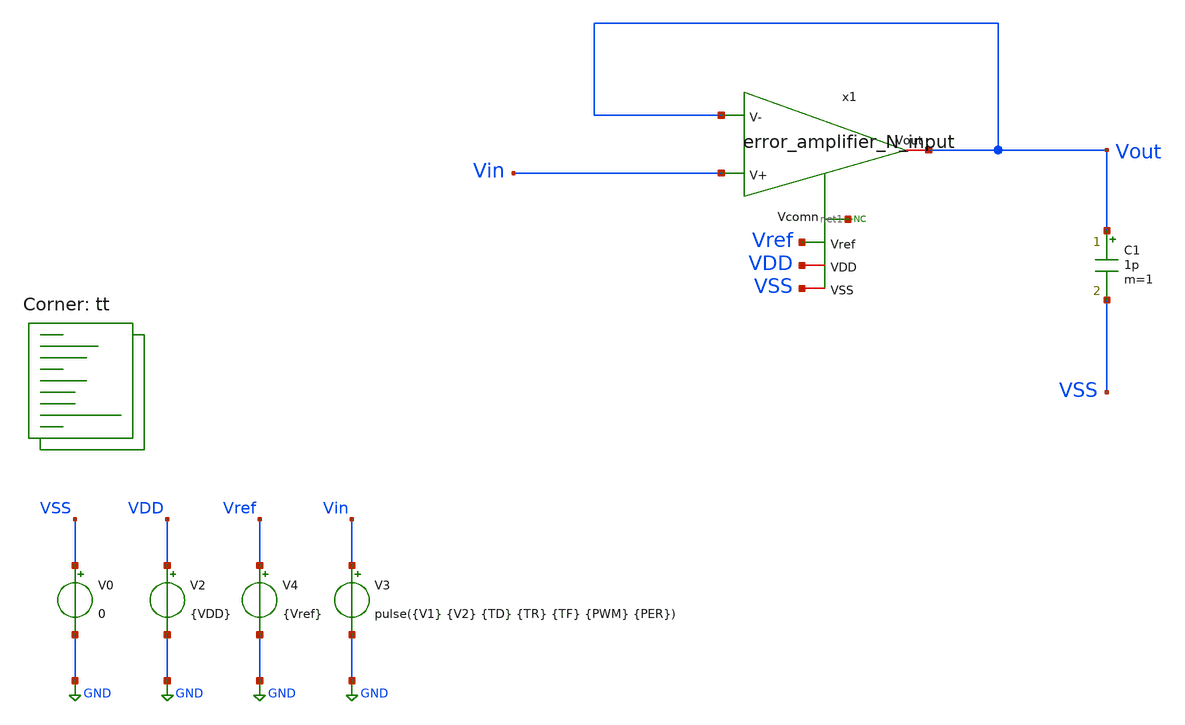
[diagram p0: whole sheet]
** sch_path: blocks/composite/folded_cascode/designs/gf180/error_amplifier_N_input/xschem/folded_cascode_sr.sch
**.subckt folded_cascode_sr
V0 VSS GND 0
V2 VDD GND {VDD}
V4 Vref GND {Vref}
C1 Vout VSS 1p m=1
* noconn #net1
V3 Vin GND pulse({V1} {V2} {TD} {TR} {TF} {PWM} {PER})
x1 Vout Vin Vout Vref VDD VSS net1 error_amplifier_N_input
**** begin user architecture code
.lib $::SKYWATER_MODELS/sky130.lib.spice tt



.param VDD=1.8
.param Vref=1.2
.param V1 = 0.01
.param V2 = 1.8
.param TR = 50n
.param TF = TR
.param PER = 2m
.param TD = 0.05*PER
.param PWM = PER/2
.save

* Operation point of the folded cascode core

*nfet
  @m.x1.x2.xm1.msky130_fd_pr__nfet_01v8[gm]  v(@m.x1.x2.xm1.msky130_fd_pr__nfet_01v8[vth])
+  @m.x1.x2.xm1.msky130_fd_pr__nfet_01v8[gds]  @m.x1.x2.xm1.msky130_fd_pr__nfet_01v8[id]
  @m.x1.x2.xm2.msky130_fd_pr__nfet_01v8[gm]  v(@m.x1.x2.xm2.msky130_fd_pr__nfet_01v8[vth])
+  @m.x1.x2.xm2.msky130_fd_pr__nfet_01v8[gds]  @m.x1.x2.xm2.msky130_fd_pr__nfet_01v8[id]
  @m.x1.x2.xm7.msky130_fd_pr__nfet_01v8[gm]  v(@m.x1.x2.xm7.msky130_fd_pr__nfet_01v8[vth])
+  @m.x1.x2.xm7.msky130_fd_pr__nfet_01v8[gds]  @m.x1.x2.xm7.msky130_fd_pr__nfet_01v8[id]
  @m.x1.x2.xm8.msky130_fd_pr__nfet_01v8[gm]  v(@m.x1.x2.xm8.msky130_fd_pr__nfet_01v8[vth])
+  @m.x1.x2.xm8.msky130_fd_pr__nfet_01v8[gds]  @m.x1.x2.xm8.msky130_fd_pr__nfet_01v8[id]
  @m.x1.x2.xm9.msky130_fd_pr__nfet_01v8[gm]  v(@m.x1.x2.xm9.msky130_fd_pr__nfet_01v8[vth])
+  @m.x1.x2.xm9.msky130_fd_pr__nfet_01v8[gds]  @m.x1.x2.xm9.msky130_fd_pr__nfet_01v8[id]
  @m.x1.x2.xm10.msky130_fd_pr__nfet_01v8[gm]  v(@m.x1.x2.xm10.msky130_fd_pr__nfet_01v8[vth])
+  @m.x1.x2.xm10.msky130_fd_pr__nfet_01v8[gds]  @m.x1.x2.xm10.msky130_fd_pr__nfet_01v8[id]
  @m.x1.x2.xm11.msky130_fd_pr__nfet_01v8[gm]  v(@m.x1.x2.xm11.msky130_fd_pr__nfet_01v8[vth])
+  @m.x1.x2.xm11.msky130_fd_pr__nfet_01v8[gds]  @m.x1.x2.xm11.msky130_fd_pr__nfet_01v8[id]

*pfet
  @m.x1.x2.xm3.msky130_fd_pr__pfet_01v8_lvt[gm]  v(@m.x1.x2.xm3.msky130_fd_pr__pfet_01v8_lvt[vth])
+  @m.x1.x2.xm3.msky130_fd_pr__pfet_01v8_lvt[gds]  @m.x1.x2.xm3.msky130_fd_pr__pfet_01v8_lvt[id]
  @m.x1.x2.xm4.msky130_fd_pr__pfet_01v8_lvt[gm]  v(@m.x1.x2.xm4.msky130_fd_pr__pfet_01v8_lvt[vth])
+  @m.x1.x2.xm4.msky130_fd_pr__pfet_01v8_lvt[gds]  @m.x1.x2.xm4.msky130_fd_pr__pfet_01v8_lvt[id]
  @m.x1.x2.xm5.msky130_fd_pr__pfet_01v8_lvt[gm]  v(@m.x1.x2.xm5.msky130_fd_pr__pfet_01v8_lvt[vth])
+  @m.x1.x2.xm5.msky130_fd_pr__pfet_01v8_lvt[gds]  @m.x1.x2.xm5.msky130_fd_pr__pfet_01v8_lvt[id]
  @m.x1.x2.xm6.msky130_fd_pr__pfet_01v8_lvt[gm]  v(@m.x1.x2.xm6.msky130_fd_pr__pfet_01v8_lvt[vth])
+  @m.x1.x2.xm6.msky130_fd_pr__pfet_01v8_lvt[gds]  @m.x1.x2.xm6.msky130_fd_pr__pfet_01v8_lvt[id]

* Operation point of the folded cascode bias

  abstol=1e-14 savecurrents
.control
    save all
    op
    remzerovec
    write folded_cascode_sr.raw
    set appendwrite

    * run ac simulation
    tran 25n 2m

    * measure parameters
    let dVout = deriv(Vout)/1e6
    meas tran SRplus MAX dVout
    meas tran SRminus MIN dVout

    meas tran Voutmax MAX Vout
    meas tran Voutmin MIN Vout
    let Output_swing = Voutmax-Voutmin
    print Output_swing

    plot Vout Vin

    write folded_cascode_sr.raw
.endc



**** end user architecture code
**.ends

* expanding   symbol:
*+  /foss/designs/chipathon_2025/designs/sky130/error_amplifier_N_input/xschem/error_amplifier_N_input.sym # of pins=7
** sym_path: blocks/composite/folded_cascode/designs/gf180/error_amplifier_N_input/xschem/error_amplifier_N_input.sym
** sch_path: blocks/composite/folded_cascode/designs/gf180/error_amplifier_N_input/xschem/error_amplifier_N_input.sch
.subckt error_amplifier_N_input Vout V+ V- Vref VDD VSS Vcomn
*.ipin V+
*.iopin Vout
*.ipin V-
*.ipin Vref
*.iopin VDD
*.iopin VSS
*.iopin Vcomn
x1 VbiasP2 VbiasN2 VbiasN1 Vout V+ V- VDD VSS Vcomn error_amplifier_core_N_input
x2 VbiasN1 VbiasN2 VbiasP2 VDD VSS Vref net1 error_amplifier_bias_N_input
* noconn #net1
.ends


* expanding   symbol:  error_amplifier_core_N_input.sym # of pins=9
** sym_path: blocks/composite/folded_cascode/designs/gf180/error_amplifier_core_N_input/xschem/error_amplifier_core_N_input.sym
** sch_path: blocks/composite/folded_cascode/designs/gf180/error_amplifier_core_N_input/xschem/error_amplifier_core_N_input.sch
.subckt error_amplifier_core_N_input VbiasP2 VbiasN2 VbiasN1 Vout V+ V- VDD VSS Vcomn
*.ipin VbiasN2
*.iopin VDD
*.ipin VbiasP2
*.ipin VbiasN1
*.ipin V+
*.ipin V-
*.iopin VSS
*.iopin Vcomn
*.iopin Vout
XM4 Vdm6 Val VDD VDD pfet_03v3 L=0.3u W=4u nf=1 ad='int((nf+1)/2) * W/nf * 0.18u' as='int((nf+2)/2) * W/nf * 0.18u'
+ pd='2*int((nf+1)/2) * (W/nf + 0.18u)' ps='2*int((nf+2)/2) * (W/nf + 0.18u)' nrd='0.18u / W' nrs='0.18u / W'
+ sa=0 sb=0 sd=0 m=12
XM3 Vdm5 Val VDD VDD pfet_03v3 L=0.3u W=4u nf=1 ad='int((nf+1)/2) * W/nf * 0.18u' as='int((nf+2)/2) * W/nf * 0.18u'
+ pd='2*int((nf+1)/2) * (W/nf + 0.18u)' ps='2*int((nf+2)/2) * (W/nf + 0.18u)' nrd='0.18u / W' nrs='0.18u / W'
+ sa=0 sb=0 sd=0 m=12
XM5 Val VbiasP2 Vdm5 VDD pfet_03v3 L=2u W=6u nf=1 ad='int((nf+1)/2) * W/nf * 0.18u' as='int((nf+2)/2) * W/nf * 0.18u'
+ pd='2*int((nf+1)/2) * (W/nf + 0.18u)' ps='2*int((nf+2)/2) * (W/nf + 0.18u)' nrd='0.18u / W' nrs='0.18u / W'
+ sa=0 sb=0 sd=0 m=2
XM6 Vout VbiasP2 Vdm6 VDD pfet_03v3 L=2u W=6u nf=1 ad='int((nf+1)/2) * W/nf * 0.18u' as='int((nf+2)/2) * W/nf * 0.18u'
+ pd='2*int((nf+1)/2) * (W/nf + 0.18u)' ps='2*int((nf+2)/2) * (W/nf + 0.18u)' nrd='0.18u / W' nrs='0.18u / W'
+ sa=0 sb=0 sd=0 m=2
XM9 net1 VbiasN1 VSS VSS nfet_03v3 L=2u W=2u nf=1 ad='int((nf+1)/2) * W/nf * 0.18u' as='int((nf+2)/2) * W/nf * 0.18u'
+ pd='2*int((nf+1)/2) * (W/nf + 0.18u)' ps='2*int((nf+2)/2) * (W/nf + 0.18u)' nrd='0.18u / W' nrs='0.18u / W'
+ sa=0 sb=0 sd=0 m=2
XM8 Vout VbiasN2 Vcomn VSS nfet_03v3 L=2u W=5u nf=1 ad='int((nf+1)/2) * W/nf * 0.18u' as='int((nf+2)/2) * W/nf * 0.18u'
+ pd='2*int((nf+1)/2) * (W/nf + 0.18u)' ps='2*int((nf+2)/2) * (W/nf + 0.18u)' nrd='0.18u / W' nrs='0.18u / W'
+ sa=0 sb=0 sd=0 m=1
XM7 Val VbiasN2 net1 VSS nfet_03v3 L=2u W=5u nf=1 ad='int((nf+1)/2) * W/nf * 0.18u' as='int((nf+2)/2) * W/nf * 0.18u'
+ pd='2*int((nf+1)/2) * (W/nf + 0.18u)' ps='2*int((nf+2)/2) * (W/nf + 0.18u)' nrd='0.18u / W' nrs='0.18u / W'
+ sa=0 sb=0 sd=0 m=1
XM10 Vcomn VbiasN1 VSS VSS nfet_03v3 L=2u W=2u nf=1 ad='int((nf+1)/2) * W/nf * 0.18u' as='int((nf+2)/2) * W/nf * 0.18u'
+ pd='2*int((nf+1)/2) * (W/nf + 0.18u)' ps='2*int((nf+2)/2) * (W/nf + 0.18u)' nrd='0.18u / W' nrs='0.18u / W'
+ sa=0 sb=0 sd=0 m=2
XM15 VDD VDD VDD VDD pfet_03v3 L=3u W=1u nf=1 ad='int((nf+1)/2) * W/nf * 0.18u' as='int((nf+2)/2) * W/nf * 0.18u'
+ pd='2*int((nf+1)/2) * (W/nf + 0.18u)' ps='2*int((nf+2)/2) * (W/nf + 0.18u)' nrd='0.18u / W' nrs='0.18u / W'
+ sa=0 sb=0 sd=0 m=28
XM16 VDD VDD VDD VDD pfet_03v3 L=1.5u W=1u nf=1 ad='int((nf+1)/2) * W/nf * 0.18u' as='int((nf+2)/2) * W/nf * 0.18u'
+ pd='2*int((nf+1)/2) * (W/nf + 0.18u)' ps='2*int((nf+2)/2) * (W/nf + 0.18u)' nrd='0.18u / W' nrs='0.18u / W'
+ sa=0 sb=0 sd=0 m=20
XM13 VSS VSS VSS VSS nfet_03v3 L=3u W=1u nf=1 ad='int((nf+1)/2) * W/nf * 0.18u' as='int((nf+2)/2) * W/nf * 0.18u'
+ pd='2*int((nf+1)/2) * (W/nf + 0.18u)' ps='2*int((nf+2)/2) * (W/nf + 0.18u)' nrd='0.18u / W' nrs='0.18u / W'
+ sa=0 sb=0 sd=0 m=18
XM12 VSS VSS VSS VSS nfet_03v3 L=6.5u W=0.5u nf=1 ad='int((nf+1)/2) * W/nf * 0.18u' as='int((nf+2)/2) * W/nf * 0.18u'
+ pd='2*int((nf+1)/2) * (W/nf + 0.18u)' ps='2*int((nf+2)/2) * (W/nf + 0.18u)' nrd='0.18u / W' nrs='0.18u / W'
+ sa=0 sb=0 sd=0 m=36
XM14 VSS VSS VSS VSS nfet_03v3 L=1u W=1u nf=1 ad='int((nf+1)/2) * W/nf * 0.18u' as='int((nf+2)/2) * W/nf * 0.18u'
+ pd='2*int((nf+1)/2) * (W/nf + 0.18u)' ps='2*int((nf+2)/2) * (W/nf + 0.18u)' nrd='0.18u / W' nrs='0.18u / W'
+ sa=0 sb=0 sd=0 m=30
XM1 Vdm6 V- net2 VSS nfet_03v3 L=1u W=10u nf=1 ad='int((nf+1)/2) * W/nf * 0.18u' as='int((nf+2)/2) * W/nf * 0.18u'
+ pd='2*int((nf+1)/2) * (W/nf + 0.18u)' ps='2*int((nf+2)/2) * (W/nf + 0.18u)' nrd='0.18u / W' nrs='0.18u / W'
+ sa=0 sb=0 sd=0 m=20
XM2 Vdm5 V+ net2 VSS nfet_03v3 L=1u W=10u nf=1 ad='int((nf+1)/2) * W/nf * 0.18u' as='int((nf+2)/2) * W/nf * 0.18u'
+ pd='2*int((nf+1)/2) * (W/nf + 0.18u)' ps='2*int((nf+2)/2) * (W/nf + 0.18u)' nrd='0.18u / W' nrs='0.18u / W'
+ sa=0 sb=0 sd=0 m=20
XM11 net2 VbiasN1 VSS VSS nfet_03v3 L=2u W=2u nf=1 ad='int((nf+1)/2) * W/nf * 0.18u' as='int((nf+2)/2) * W/nf * 0.18u'
+ pd='2*int((nf+1)/2) * (W/nf + 0.18u)' ps='2*int((nf+2)/2) * (W/nf + 0.18u)' nrd='0.18u / W' nrs='0.18u / W'
+ sa=0 sb=0 sd=0 m=40
.ends


* expanding   symbol:  error_amplifier_bias_N_input.sym # of pins=7
** sym_path: blocks/composite/folded_cascode/designs/gf180/error_amplifier_bias_N_input/xschem/error_amplifier_bias_N_input.sym
** sch_path: blocks/composite/folded_cascode/designs/gf180/error_amplifier_bias_N_input/xschem/error_amplifier_bias_N_input.sch
.subckt error_amplifier_bias_N_input VbiasN1 VbiasN2 VbiasP2 VDD VSS Vref VbiasP1
*.ipin Vref
*.iopin VbiasN1
*.iopin VbiasN2
*.iopin VDD
*.iopin VbiasP2
*.iopin VSS
*.iopin VbiasP1
XM1 VbiasN2 VbiasN2 net2 VSS nfet_03v3 L=6u W=0.5u nf=1 ad='int((nf+1)/2) * W/nf * 0.18u' as='int((nf+2)/2) * W/nf * 0.18u'
+ pd='2*int((nf+1)/2) * (W/nf + 0.18u)' ps='2*int((nf+2)/2) * (W/nf + 0.18u)' nrd='0.18u / W' nrs='0.18u / W'
+ sa=0 sb=0 sd=0 m=1
XM2 VbiasP1 VbiasP1 VDD VDD pfet_03v3 L=2u W=0.5u nf=1 ad='int((nf+1)/2) * W/nf * 0.18u' as='int((nf+2)/2) * W/nf * 0.18u'
+ pd='2*int((nf+1)/2) * (W/nf + 0.18u)' ps='2*int((nf+2)/2) * (W/nf + 0.18u)' nrd='0.18u / W' nrs='0.18u / W'
+ sa=0 sb=0 sd=0 m=1
XM3 VbiasP1 Vref net1 VSS nfet_03v3 L=6u W=0.5u nf=1 ad='int((nf+1)/2) * W/nf * 0.18u' as='int((nf+2)/2) * W/nf * 0.18u'
+ pd='2*int((nf+1)/2) * (W/nf + 0.18u)' ps='2*int((nf+2)/2) * (W/nf + 0.18u)' nrd='0.18u / W' nrs='0.18u / W'
+ sa=0 sb=0 sd=0 m=1
XM4 VbiasN2 VbiasP1 VDD VDD pfet_03v3 L=2u W=0.5u nf=1 ad='int((nf+1)/2) * W/nf * 0.18u' as='int((nf+2)/2) * W/nf * 0.18u'
+ pd='2*int((nf+1)/2) * (W/nf + 0.18u)' ps='2*int((nf+2)/2) * (W/nf + 0.18u)' nrd='0.18u / W' nrs='0.18u / W'
+ sa=0 sb=0 sd=0 m=1
XM5 VbiasN1 VbiasP1 VDD VDD pfet_03v3 L=2u W=0.5u nf=1 ad='int((nf+1)/2) * W/nf * 0.18u' as='int((nf+2)/2) * W/nf * 0.18u'
+ pd='2*int((nf+1)/2) * (W/nf + 0.18u)' ps='2*int((nf+2)/2) * (W/nf + 0.18u)' nrd='0.18u / W' nrs='0.18u / W'
+ sa=0 sb=0 sd=0 m=1
XM6 net6 VbiasP2 VDD VDD pfet_03v3 L=2u W=0.5u nf=1 ad='int((nf+1)/2) * W/nf * 0.18u' as='int((nf+2)/2) * W/nf * 0.18u'
+ pd='2*int((nf+1)/2) * (W/nf + 0.18u)' ps='2*int((nf+2)/2) * (W/nf + 0.18u)' nrd='0.18u / W' nrs='0.18u / W'
+ sa=0 sb=0 sd=0 m=1
XM7 VbiasP2 VbiasP2 net6 VDD pfet_03v3 L=2u W=0.5u nf=1 ad='int((nf+1)/2) * W/nf * 0.18u' as='int((nf+2)/2) * W/nf * 0.18u'
+ pd='2*int((nf+1)/2) * (W/nf + 0.18u)' ps='2*int((nf+2)/2) * (W/nf + 0.18u)' nrd='0.18u / W' nrs='0.18u / W'
+ sa=0 sb=0 sd=0 m=1
XM8 net7 net8 VDD VDD pfet_03v3 L=2u W=0.5u nf=1 ad='int((nf+1)/2) * W/nf * 0.18u' as='int((nf+2)/2) * W/nf * 0.18u'
+ pd='2*int((nf+1)/2) * (W/nf + 0.18u)' ps='2*int((nf+2)/2) * (W/nf + 0.18u)' nrd='0.18u / W' nrs='0.18u / W'
+ sa=0 sb=0 sd=0 m=3
XM9 net8 VbiasP2 net7 VDD pfet_03v3 L=2u W=0.5u nf=1 ad='int((nf+1)/2) * W/nf * 0.18u' as='int((nf+2)/2) * W/nf * 0.18u'
+ pd='2*int((nf+1)/2) * (W/nf + 0.18u)' ps='2*int((nf+2)/2) * (W/nf + 0.18u)' nrd='0.18u / W' nrs='0.18u / W'
+ sa=0 sb=0 sd=0 m=2
XM10 net10 VbiasN1 VSS VSS nfet_03v3 L=6u W=0.5u nf=1 ad='int((nf+1)/2) * W/nf * 0.18u' as='int((nf+2)/2) * W/nf * 0.18u'
+ pd='2*int((nf+1)/2) * (W/nf + 0.18u)' ps='2*int((nf+2)/2) * (W/nf + 0.18u)' nrd='0.18u / W' nrs='0.18u / W'
+ sa=0 sb=0 sd=0 m=4
XM11 VbiasN1 VbiasN2 net3 VSS nfet_03v3 L=6u W=0.5u nf=1 ad='int((nf+1)/2) * W/nf * 0.18u' as='int((nf+2)/2) * W/nf * 0.18u'
+ pd='2*int((nf+1)/2) * (W/nf + 0.18u)' ps='2*int((nf+2)/2) * (W/nf + 0.18u)' nrd='0.18u / W' nrs='0.18u / W'
+ sa=0 sb=0 sd=0 m=5
XM12 VbiasP2 VbiasN2 net4 VSS nfet_03v3 L=6u W=0.5u nf=1 ad='int((nf+1)/2) * W/nf * 0.18u' as='int((nf+2)/2) * W/nf * 0.18u'
+ pd='2*int((nf+1)/2) * (W/nf + 0.18u)' ps='2*int((nf+2)/2) * (W/nf + 0.18u)' nrd='0.18u / W' nrs='0.18u / W'
+ sa=0 sb=0 sd=0 m=5
XM13 net8 VbiasN2 net9 VSS nfet_03v3 L=6u W=0.5u nf=1 ad='int((nf+1)/2) * W/nf * 0.18u' as='int((nf+2)/2) * W/nf * 0.18u'
+ pd='2*int((nf+1)/2) * (W/nf + 0.18u)' ps='2*int((nf+2)/2) * (W/nf + 0.18u)' nrd='0.18u / W' nrs='0.18u / W'
+ sa=0 sb=0 sd=0 m=5
XM14 net2 VbiasN2 VSS VSS nfet_03v3 L=6u W=0.5u nf=1 ad='int((nf+1)/2) * W/nf * 0.18u' as='int((nf+2)/2) * W/nf * 0.18u'
+ pd='2*int((nf+1)/2) * (W/nf + 0.18u)' ps='2*int((nf+2)/2) * (W/nf + 0.18u)' nrd='0.18u / W' nrs='0.18u / W'
+ sa=0 sb=0 sd=0 m=1
XM15 net3 VbiasN1 net11 VSS nfet_03v3 L=6u W=0.5u nf=1 ad='int((nf+1)/2) * W/nf * 0.18u' as='int((nf+2)/2) * W/nf * 0.18u'
+ pd='2*int((nf+1)/2) * (W/nf + 0.18u)' ps='2*int((nf+2)/2) * (W/nf + 0.18u)' nrd='0.18u / W' nrs='0.18u / W'
+ sa=0 sb=0 sd=0 m=4
XM16 net4 VbiasN1 net5 VSS nfet_03v3 L=6u W=0.5u nf=1 ad='int((nf+1)/2) * W/nf * 0.18u' as='int((nf+2)/2) * W/nf * 0.18u'
+ pd='2*int((nf+1)/2) * (W/nf + 0.18u)' ps='2*int((nf+2)/2) * (W/nf + 0.18u)' nrd='0.18u / W' nrs='0.18u / W'
+ sa=0 sb=0 sd=0 m=4
XM17 net9 VbiasN1 net10 VSS nfet_03v3 L=6u W=0.5u nf=1 ad='int((nf+1)/2) * W/nf * 0.18u' as='int((nf+2)/2) * W/nf * 0.18u'
+ pd='2*int((nf+1)/2) * (W/nf + 0.18u)' ps='2*int((nf+2)/2) * (W/nf + 0.18u)' nrd='0.18u / W' nrs='0.18u / W'
+ sa=0 sb=0 sd=0 m=4
XM18 net1 Vref VSS VSS nfet_03v3 L=6u W=0.5u nf=1 ad='int((nf+1)/2) * W/nf * 0.18u' as='int((nf+2)/2) * W/nf * 0.18u'
+ pd='2*int((nf+1)/2) * (W/nf + 0.18u)' ps='2*int((nf+2)/2) * (W/nf + 0.18u)' nrd='0.18u / W' nrs='0.18u / W'
+ sa=0 sb=0 sd=0 m=1
XM19 net5 VbiasN1 VSS VSS nfet_03v3 L=6u W=0.5u nf=1 ad='int((nf+1)/2) * W/nf * 0.18u' as='int((nf+2)/2) * W/nf * 0.18u'
+ pd='2*int((nf+1)/2) * (W/nf + 0.18u)' ps='2*int((nf+2)/2) * (W/nf + 0.18u)' nrd='0.18u / W' nrs='0.18u / W'
+ sa=0 sb=0 sd=0 m=4
XM20 net11 VbiasN1 VSS VSS nfet_03v3 L=6u W=0.5u nf=1 ad='int((nf+1)/2) * W/nf * 0.18u' as='int((nf+2)/2) * W/nf * 0.18u'
+ pd='2*int((nf+1)/2) * (W/nf + 0.18u)' ps='2*int((nf+2)/2) * (W/nf + 0.18u)' nrd='0.18u / W' nrs='0.18u / W'
+ sa=0 sb=0 sd=0 m=4
.ends

.GLOBAL GND
.end
